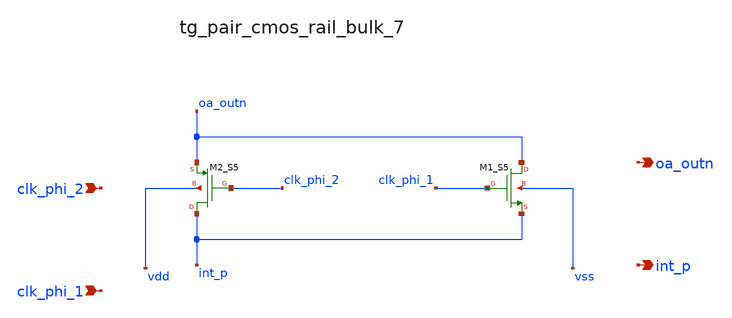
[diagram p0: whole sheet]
** sch_path: analog-db/raw/sup_003_rrl_sc_integrator/hier/blocks/tg_pair_cmos_rail_bulk_7.sch
**.subckt tg_pair_cmos_rail_bulk_7 clk_phi_2 clk_phi_1 oa_outn int_p
*.ipin clk_phi_2
*.ipin clk_phi_1
*.opin oa_outn
*.opin int_p
XM1_S5 oa_outn clk_phi_1 int_p vss sg13_lv_nmos w=x_dut_xm1_s5_w l=x_dut_xm1_s5_l ng=1
+ m=x_dut_xm1_s5_m
XM2_S5 int_p clk_phi_2 oa_outn vdd sg13_lv_pmos w=x_dut_xm2_s5_w l=x_dut_xm2_s5_l ng=1
+ m=x_dut_xm2_s5_m
**.ends
.end
